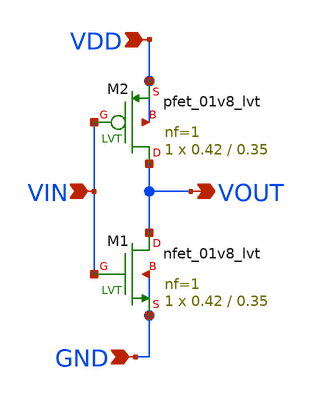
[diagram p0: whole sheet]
** sch_path: design/LELO_SVOD_SKY130A/LELO_RING_DEL.sch
**.subckt LELO_RING_DEL VIN VDD GND VOUT
*.ipin VIN
*.ipin VDD
*.ipin GND
*.opin VOUT
XM1 VOUT VIN GND GND sky130_fd_pr__nfet_01v8_lvt L=0.35 W=0.42 nf=1 ad='int((1 + 1)/2) * 0.42 / 1 * 0.29'
+ as='int((1 + 2)/2) * 0.42 / 1 * 0.29' pd='2*int((1 + 1)/2) * (0.42 / 1 + 0.29)' ps='2*int((1 + 2)/2) * (0.42 / 1 + 0.29)'
+ nrd='0.29 / 0.42 ' nrs='0.29 / 0.42 ' sa=0 sb=0 sd=0 mult=1 m=1
XM2 VOUT VIN VDD VDD sky130_fd_pr__pfet_01v8_lvt L=0.35 W=0.42 nf=1 ad='int((1 + 1)/2) * 0.42 / 1 * 0.29'
+ as='int((1 + 2)/2) * 0.42 / 1 * 0.29' pd='2*int((1 + 1)/2) * (0.42 / 1 + 0.29)' ps='2*int((1 + 2)/2) * (0.42 / 1 + 0.29)'
+ nrd='0.29 / 0.42 ' nrs='0.29 / 0.42 ' sa=0 sb=0 sd=0 mult=1 m=1
**.ends
.end
